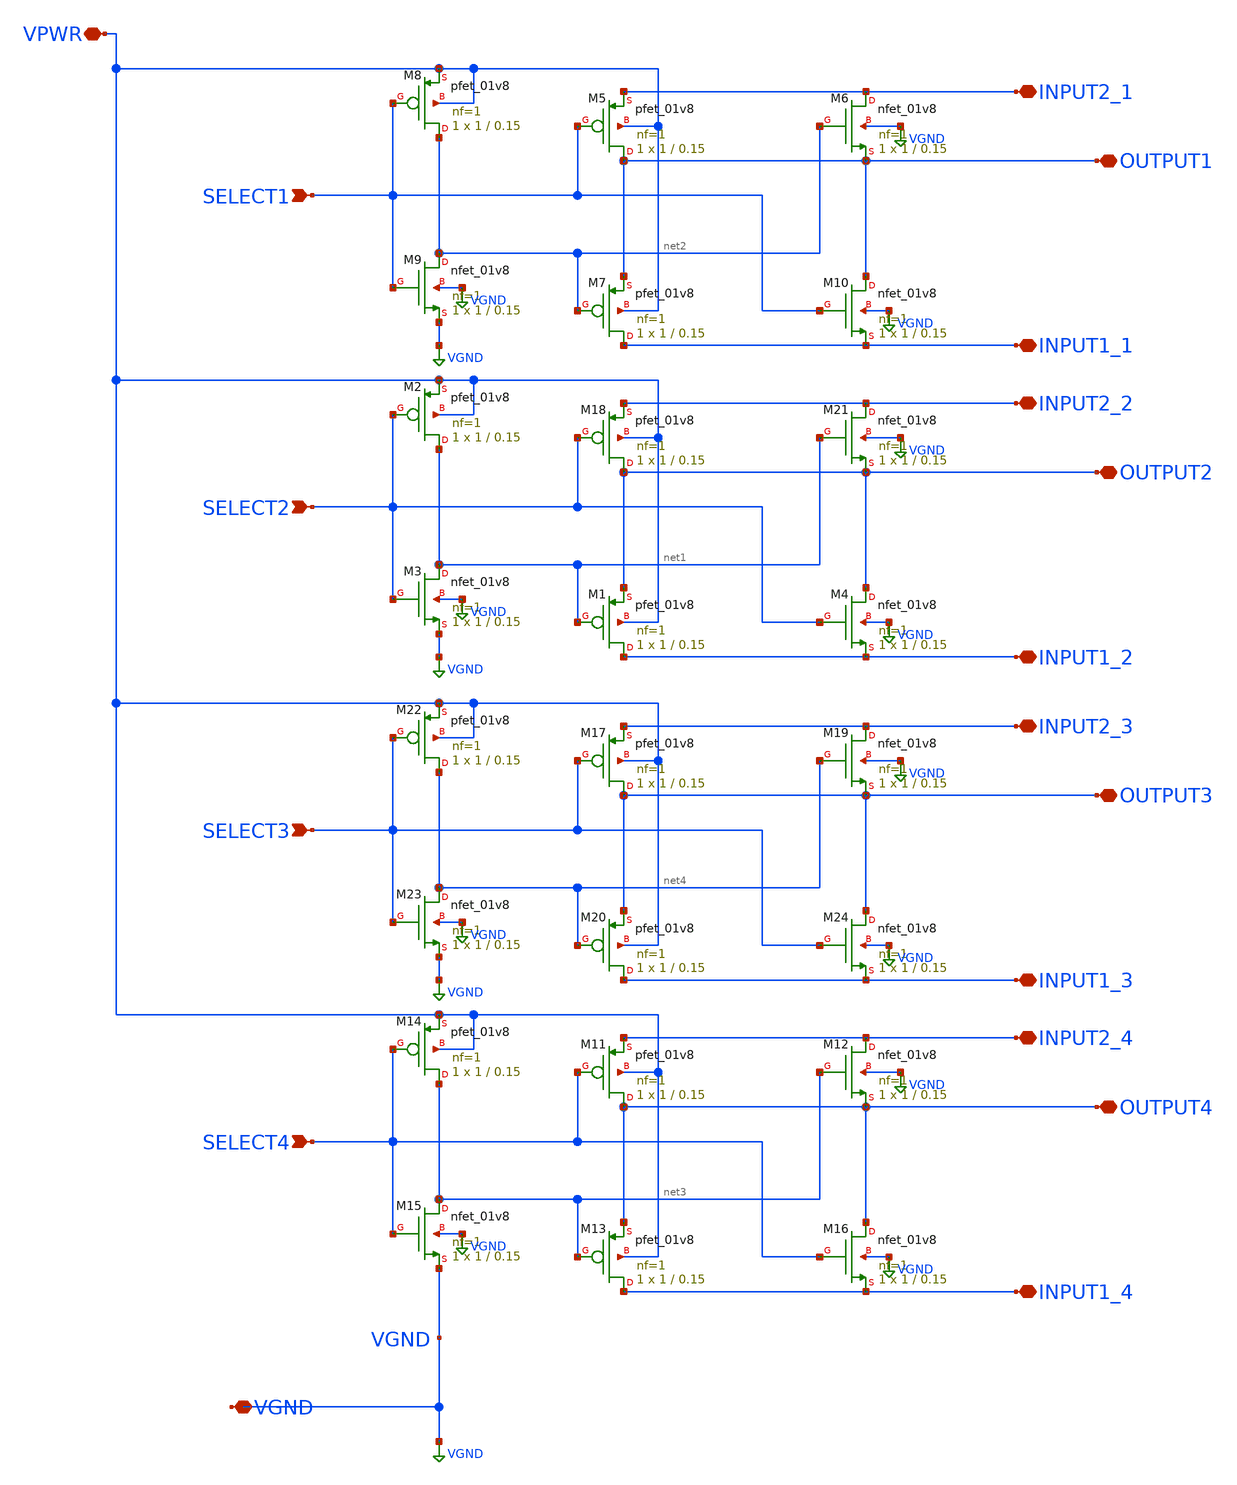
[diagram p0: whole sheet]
** sch_path: libs.ref/sky130_hilas_sc/xschem/sky130_hilas_Tgate4Double01.sch
**.subckt sky130_hilas_Tgate4Double01 SELECT2 VPWR INPUT1_2 OUTPUT2 INPUT2_2 SELECT1 INPUT1_1
*+ OUTPUT1 INPUT2_1 SELECT4 INPUT1_4 OUTPUT4 INPUT2_4 SELECT3 INPUT1_3 OUTPUT3 INPUT2_3 VGND
*.ipin SELECT2
*.iopin VPWR
*.iopin INPUT1_2
*.iopin OUTPUT2
*.iopin INPUT2_2
*.ipin SELECT1
*.iopin INPUT1_1
*.iopin OUTPUT1
*.iopin INPUT2_1
*.ipin SELECT4
*.iopin INPUT1_4
*.iopin OUTPUT4
*.iopin INPUT2_4
*.ipin SELECT3
*.iopin INPUT1_3
*.iopin OUTPUT3
*.iopin INPUT2_3
*.iopin VGND
XM18 OUTPUT2 SELECT2 INPUT2_2 VPWR sky130_fd_pr__pfet_01v8 L=0.15 W=1 nf=1 ad='int((nf+1)/2) * W/nf * 0.29'
+ as='int((nf+2)/2) * W/nf * 0.29' pd='2*int((nf+1)/2) * (W/nf + 0.29)' ps='2*int((nf+2)/2) * (W/nf + 0.29)'
+ nrd='0.29 / W' nrs='0.29 / W' sa=0 sb=0 sd=0 mult=1 m=1
XM21 INPUT2_2 net1 OUTPUT2 VGND sky130_fd_pr__nfet_01v8 L=0.15 W=1 nf=1 ad='int((nf+1)/2) * W/nf * 0.29'
+ as='int((nf+2)/2) * W/nf * 0.29' pd='2*int((nf+1)/2) * (W/nf + 0.29)' ps='2*int((nf+2)/2) * (W/nf + 0.29)'
+ nrd='0.29 / W' nrs='0.29 / W' sa=0 sb=0 sd=0 mult=1 m=1
XM1 INPUT1_2 net1 OUTPUT2 VPWR sky130_fd_pr__pfet_01v8 L=0.15 W=1 nf=1 ad='int((nf+1)/2) * W/nf * 0.29'
+ as='int((nf+2)/2) * W/nf * 0.29' pd='2*int((nf+1)/2) * (W/nf + 0.29)' ps='2*int((nf+2)/2) * (W/nf + 0.29)'
+ nrd='0.29 / W' nrs='0.29 / W' sa=0 sb=0 sd=0 mult=1 m=1
XM2 net1 SELECT2 VPWR VPWR sky130_fd_pr__pfet_01v8 L=0.15 W=1 nf=1 ad='int((nf+1)/2) * W/nf * 0.29' as='int((nf+2)/2) * W/nf * 0.29'
+ pd='2*int((nf+1)/2) * (W/nf + 0.29)' ps='2*int((nf+2)/2) * (W/nf + 0.29)' nrd='0.29 / W' nrs='0.29 / W'
+ sa=0 sb=0 sd=0 mult=1 m=1
XM3 net1 SELECT2 VGND VGND sky130_fd_pr__nfet_01v8 L=0.15 W=1 nf=1 ad='int((nf+1)/2) * W/nf * 0.29' as='int((nf+2)/2) * W/nf * 0.29'
+ pd='2*int((nf+1)/2) * (W/nf + 0.29)' ps='2*int((nf+2)/2) * (W/nf + 0.29)' nrd='0.29 / W' nrs='0.29 / W'
+ sa=0 sb=0 sd=0 mult=1 m=1
XM4 OUTPUT2 SELECT2 INPUT1_2 VGND sky130_fd_pr__nfet_01v8 L=0.15 W=1 nf=1 ad='int((nf+1)/2) * W/nf * 0.29'
+ as='int((nf+2)/2) * W/nf * 0.29' pd='2*int((nf+1)/2) * (W/nf + 0.29)' ps='2*int((nf+2)/2) * (W/nf + 0.29)'
+ nrd='0.29 / W' nrs='0.29 / W' sa=0 sb=0 sd=0 mult=1 m=1
XM5 OUTPUT1 SELECT1 INPUT2_1 VPWR sky130_fd_pr__pfet_01v8 L=0.15 W=1 nf=1 ad='int((nf+1)/2) * W/nf * 0.29'
+ as='int((nf+2)/2) * W/nf * 0.29' pd='2*int((nf+1)/2) * (W/nf + 0.29)' ps='2*int((nf+2)/2) * (W/nf + 0.29)'
+ nrd='0.29 / W' nrs='0.29 / W' sa=0 sb=0 sd=0 mult=1 m=1
XM6 INPUT2_1 net2 OUTPUT1 VGND sky130_fd_pr__nfet_01v8 L=0.15 W=1 nf=1 ad='int((nf+1)/2) * W/nf * 0.29'
+ as='int((nf+2)/2) * W/nf * 0.29' pd='2*int((nf+1)/2) * (W/nf + 0.29)' ps='2*int((nf+2)/2) * (W/nf + 0.29)'
+ nrd='0.29 / W' nrs='0.29 / W' sa=0 sb=0 sd=0 mult=1 m=1
XM7 INPUT1_1 net2 OUTPUT1 VPWR sky130_fd_pr__pfet_01v8 L=0.15 W=1 nf=1 ad='int((nf+1)/2) * W/nf * 0.29'
+ as='int((nf+2)/2) * W/nf * 0.29' pd='2*int((nf+1)/2) * (W/nf + 0.29)' ps='2*int((nf+2)/2) * (W/nf + 0.29)'
+ nrd='0.29 / W' nrs='0.29 / W' sa=0 sb=0 sd=0 mult=1 m=1
XM8 net2 SELECT1 VPWR VPWR sky130_fd_pr__pfet_01v8 L=0.15 W=1 nf=1 ad='int((nf+1)/2) * W/nf * 0.29' as='int((nf+2)/2) * W/nf * 0.29'
+ pd='2*int((nf+1)/2) * (W/nf + 0.29)' ps='2*int((nf+2)/2) * (W/nf + 0.29)' nrd='0.29 / W' nrs='0.29 / W'
+ sa=0 sb=0 sd=0 mult=1 m=1
XM9 net2 SELECT1 VGND VGND sky130_fd_pr__nfet_01v8 L=0.15 W=1 nf=1 ad='int((nf+1)/2) * W/nf * 0.29' as='int((nf+2)/2) * W/nf * 0.29'
+ pd='2*int((nf+1)/2) * (W/nf + 0.29)' ps='2*int((nf+2)/2) * (W/nf + 0.29)' nrd='0.29 / W' nrs='0.29 / W'
+ sa=0 sb=0 sd=0 mult=1 m=1
XM10 OUTPUT1 SELECT1 INPUT1_1 VGND sky130_fd_pr__nfet_01v8 L=0.15 W=1 nf=1 ad='int((nf+1)/2) * W/nf * 0.29'
+ as='int((nf+2)/2) * W/nf * 0.29' pd='2*int((nf+1)/2) * (W/nf + 0.29)' ps='2*int((nf+2)/2) * (W/nf + 0.29)'
+ nrd='0.29 / W' nrs='0.29 / W' sa=0 sb=0 sd=0 mult=1 m=1
XM11 OUTPUT4 SELECT4 INPUT2_4 VPWR sky130_fd_pr__pfet_01v8 L=0.15 W=1 nf=1 ad='int((nf+1)/2) * W/nf * 0.29'
+ as='int((nf+2)/2) * W/nf * 0.29' pd='2*int((nf+1)/2) * (W/nf + 0.29)' ps='2*int((nf+2)/2) * (W/nf + 0.29)'
+ nrd='0.29 / W' nrs='0.29 / W' sa=0 sb=0 sd=0 mult=1 m=1
XM12 INPUT2_4 net3 OUTPUT4 VGND sky130_fd_pr__nfet_01v8 L=0.15 W=1 nf=1 ad='int((nf+1)/2) * W/nf * 0.29'
+ as='int((nf+2)/2) * W/nf * 0.29' pd='2*int((nf+1)/2) * (W/nf + 0.29)' ps='2*int((nf+2)/2) * (W/nf + 0.29)'
+ nrd='0.29 / W' nrs='0.29 / W' sa=0 sb=0 sd=0 mult=1 m=1
XM13 INPUT1_4 net3 OUTPUT4 VPWR sky130_fd_pr__pfet_01v8 L=0.15 W=1 nf=1 ad='int((nf+1)/2) * W/nf * 0.29'
+ as='int((nf+2)/2) * W/nf * 0.29' pd='2*int((nf+1)/2) * (W/nf + 0.29)' ps='2*int((nf+2)/2) * (W/nf + 0.29)'
+ nrd='0.29 / W' nrs='0.29 / W' sa=0 sb=0 sd=0 mult=1 m=1
XM14 net3 SELECT4 VPWR VPWR sky130_fd_pr__pfet_01v8 L=0.15 W=1 nf=1 ad='int((nf+1)/2) * W/nf * 0.29'
+ as='int((nf+2)/2) * W/nf * 0.29' pd='2*int((nf+1)/2) * (W/nf + 0.29)' ps='2*int((nf+2)/2) * (W/nf + 0.29)'
+ nrd='0.29 / W' nrs='0.29 / W' sa=0 sb=0 sd=0 mult=1 m=1
XM15 net3 SELECT4 VGND VGND sky130_fd_pr__nfet_01v8 L=0.15 W=1 nf=1 ad='int((nf+1)/2) * W/nf * 0.29'
+ as='int((nf+2)/2) * W/nf * 0.29' pd='2*int((nf+1)/2) * (W/nf + 0.29)' ps='2*int((nf+2)/2) * (W/nf + 0.29)'
+ nrd='0.29 / W' nrs='0.29 / W' sa=0 sb=0 sd=0 mult=1 m=1
XM16 OUTPUT4 SELECT4 INPUT1_4 VGND sky130_fd_pr__nfet_01v8 L=0.15 W=1 nf=1 ad='int((nf+1)/2) * W/nf * 0.29'
+ as='int((nf+2)/2) * W/nf * 0.29' pd='2*int((nf+1)/2) * (W/nf + 0.29)' ps='2*int((nf+2)/2) * (W/nf + 0.29)'
+ nrd='0.29 / W' nrs='0.29 / W' sa=0 sb=0 sd=0 mult=1 m=1
XM17 OUTPUT3 SELECT3 INPUT2_3 VPWR sky130_fd_pr__pfet_01v8 L=0.15 W=1 nf=1 ad='int((nf+1)/2) * W/nf * 0.29'
+ as='int((nf+2)/2) * W/nf * 0.29' pd='2*int((nf+1)/2) * (W/nf + 0.29)' ps='2*int((nf+2)/2) * (W/nf + 0.29)'
+ nrd='0.29 / W' nrs='0.29 / W' sa=0 sb=0 sd=0 mult=1 m=1
XM19 INPUT2_3 net4 OUTPUT3 VGND sky130_fd_pr__nfet_01v8 L=0.15 W=1 nf=1 ad='int((nf+1)/2) * W/nf * 0.29'
+ as='int((nf+2)/2) * W/nf * 0.29' pd='2*int((nf+1)/2) * (W/nf + 0.29)' ps='2*int((nf+2)/2) * (W/nf + 0.29)'
+ nrd='0.29 / W' nrs='0.29 / W' sa=0 sb=0 sd=0 mult=1 m=1
XM20 INPUT1_3 net4 OUTPUT3 VPWR sky130_fd_pr__pfet_01v8 L=0.15 W=1 nf=1 ad='int((nf+1)/2) * W/nf * 0.29'
+ as='int((nf+2)/2) * W/nf * 0.29' pd='2*int((nf+1)/2) * (W/nf + 0.29)' ps='2*int((nf+2)/2) * (W/nf + 0.29)'
+ nrd='0.29 / W' nrs='0.29 / W' sa=0 sb=0 sd=0 mult=1 m=1
XM22 net4 SELECT3 VPWR VPWR sky130_fd_pr__pfet_01v8 L=0.15 W=1 nf=1 ad='int((nf+1)/2) * W/nf * 0.29'
+ as='int((nf+2)/2) * W/nf * 0.29' pd='2*int((nf+1)/2) * (W/nf + 0.29)' ps='2*int((nf+2)/2) * (W/nf + 0.29)'
+ nrd='0.29 / W' nrs='0.29 / W' sa=0 sb=0 sd=0 mult=1 m=1
XM23 net4 SELECT3 VGND VGND sky130_fd_pr__nfet_01v8 L=0.15 W=1 nf=1 ad='int((nf+1)/2) * W/nf * 0.29'
+ as='int((nf+2)/2) * W/nf * 0.29' pd='2*int((nf+1)/2) * (W/nf + 0.29)' ps='2*int((nf+2)/2) * (W/nf + 0.29)'
+ nrd='0.29 / W' nrs='0.29 / W' sa=0 sb=0 sd=0 mult=1 m=1
XM24 OUTPUT3 SELECT3 INPUT1_3 VGND sky130_fd_pr__nfet_01v8 L=0.15 W=1 nf=1 ad='int((nf+1)/2) * W/nf * 0.29'
+ as='int((nf+2)/2) * W/nf * 0.29' pd='2*int((nf+1)/2) * (W/nf + 0.29)' ps='2*int((nf+2)/2) * (W/nf + 0.29)'
+ nrd='0.29 / W' nrs='0.29 / W' sa=0 sb=0 sd=0 mult=1 m=1
**.ends
.GLOBAL VGND
.end
